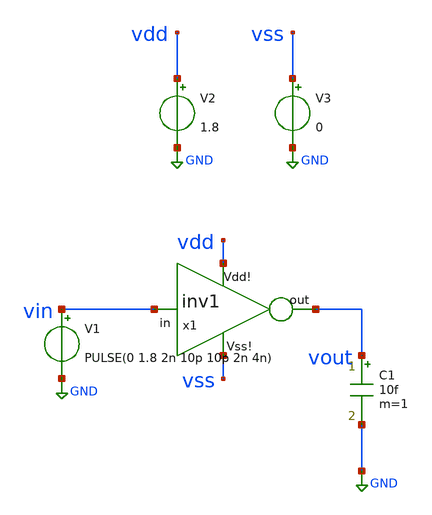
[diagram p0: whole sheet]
** sch_path: inverter_simulation/sim_inv1.sch
**.subckt sim_inv1
x1 vdd vin vout vss inv1
C1 vout GND 10f m=1
V1 vin GND PULSE(0 1.8 2n 10p 10p 2n 4n)
V2 vdd GND 1.8
V3 vss GND 0
**** begin user architecture code



.lib ~/tecnicas_digitales_programas/open_pdks/sky130/sky130A/libs.tech/ngspice/sky130.lib.spice tt

.control
set color0 = rgb:f/f/e
tran 0.01ns 5n
plot vin vout
.endc

.save all



**** end user architecture code
**.ends

* expanding   symbol:  inv1.sym # of pins=4
** sym_path: inverter_simulation/inv1.sym
** sch_path: inverter_simulation/inv1.sch
.subckt inv1 Vdd! in out Vss!
*.iopin Vdd!
*.iopin Vss!
*.ipin in
*.opin out
XM1 out in Vss! Vss! sky130_fd_pr__nfet_01v8 L=0.15 W=0.65 nf=1 ad='int((nf+1)/2) * W/nf * 0.29' as='int((nf+2)/2) * W/nf * 0.29'
+ pd='2*int((nf+1)/2) * (W/nf + 0.29)' ps='2*int((nf+2)/2) * (W/nf + 0.29)' nrd='0.29 / W' nrs='0.29 / W'
+ sa=0 sb=0 sd=0 mult=1 m=1
XM3 out in Vdd! Vdd! sky130_fd_pr__pfet_01v8 L=0.15 W=1 nf=1 ad='int((nf+1)/2) * W/nf * 0.29' as='int((nf+2)/2) * W/nf * 0.29'
+ pd='2*int((nf+1)/2) * (W/nf + 0.29)' ps='2*int((nf+2)/2) * (W/nf + 0.29)' nrd='0.29 / W' nrs='0.29 / W'
+ sa=0 sb=0 sd=0 mult=1 m=1
.ends

.GLOBAL GND
.end
